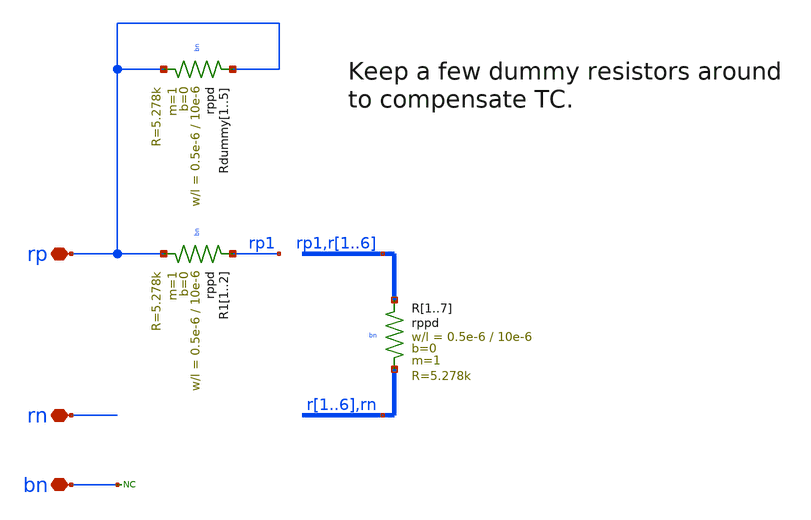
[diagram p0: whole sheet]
** sch_path: xschem/bandgap_simple_res-37k5.sch
* (c) 2025 Harald Pretl, Apache-2.0 license
**.subckt bandgap_simple_res-37k5 rp rn bn
*.iopin rp
*.iopin rn
*.iopin bn
XR1 rp1 r1 bn rppd w=0.5e-6 l=10e-6 m=1 b=0 mm_ok=1
XR2 r1 r2 bn rppd w=0.5e-6 l=10e-6 m=1 b=0 mm_ok=1
XR3 r2 r3 bn rppd w=0.5e-6 l=10e-6 m=1 b=0 mm_ok=1
XR4 r3 r4 bn rppd w=0.5e-6 l=10e-6 m=1 b=0 mm_ok=1
XR5 r4 r5 bn rppd w=0.5e-6 l=10e-6 m=1 b=0 mm_ok=1
XR6 r5 r6 bn rppd w=0.5e-6 l=10e-6 m=1 b=0 mm_ok=1
XR7 r6 rn bn rppd w=0.5e-6 l=10e-6 m=1 b=0 mm_ok=1
XR11 rp1 rp bn rppd w=0.5e-6 l=10e-6 m=1 b=0 mm_ok=1
XR12 rp1 rp bn rppd w=0.5e-6 l=10e-6 m=1 b=0 mm_ok=1
XRdummy1 rp rp bn rppd w=0.5e-6 l=10e-6 m=1 b=0 mm_ok=1
XRdummy2 rp rp bn rppd w=0.5e-6 l=10e-6 m=1 b=0 mm_ok=1
XRdummy3 rp rp bn rppd w=0.5e-6 l=10e-6 m=1 b=0 mm_ok=1
XRdummy4 rp rp bn rppd w=0.5e-6 l=10e-6 m=1 b=0 mm_ok=1
XRdummy5 rp rp bn rppd w=0.5e-6 l=10e-6 m=1 b=0 mm_ok=1
* noconn bn
**.ends
.end
